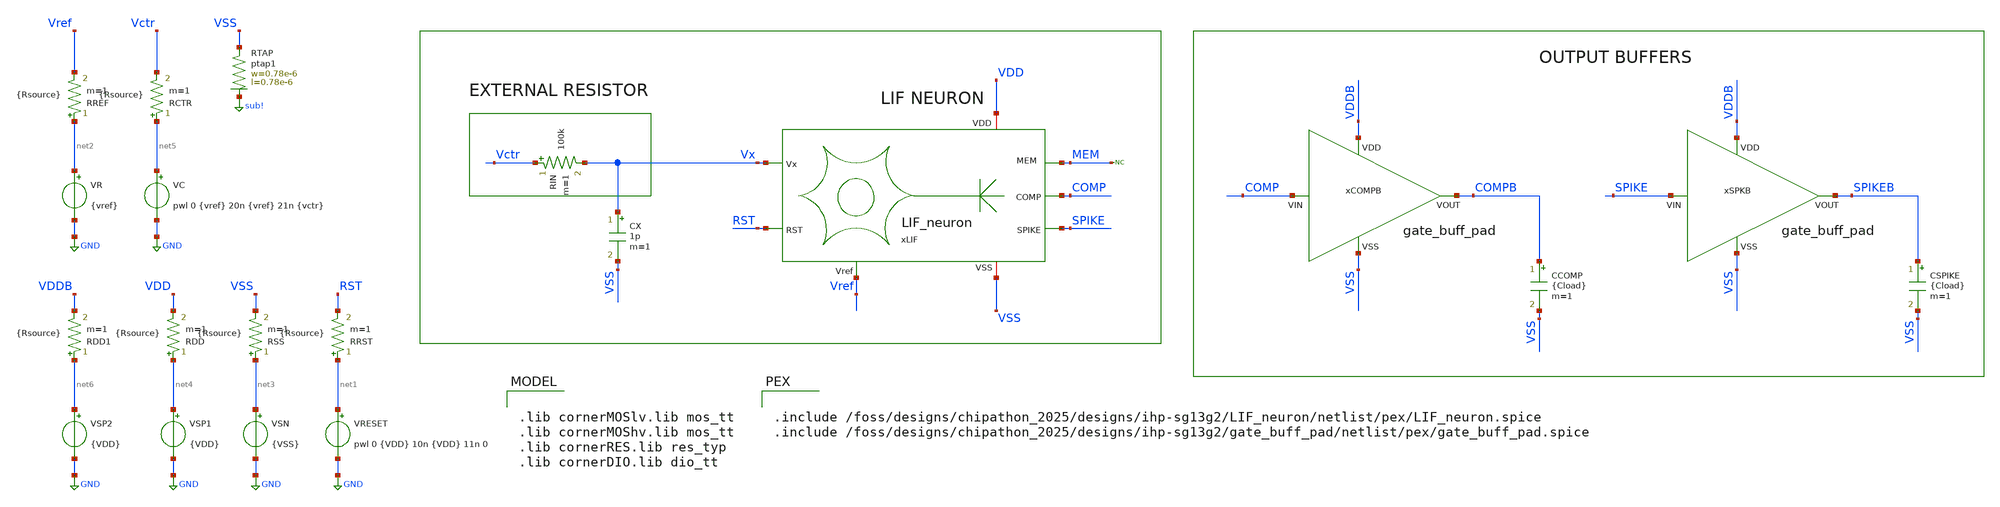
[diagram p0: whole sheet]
** sch_path: work/LIF_neuron/xschem/LIF_Neuron_tb_current.sch
**.subckt LIF_Neuron_tb_current
VRESET net1 GND pwl 0 {VDD} 10n {VDD} 11n 0
VSN net3 GND {VSS}
VR net2 GND {vref}
VC net5 GND pwl 0 {vref} 20n {vref} 21n {vctr}
xLIF VDD Vx MEM RST SPIKE VSS Vref COMP LIF_neuron
RDD net4 VDD {Rsource} m=1
RSS net3 VSS {Rsource} m=1
RRST net1 RST {Rsource} m=1
RREF net2 Vref {Rsource} m=1
RCTR net5 Vctr {Rsource} m=1
CSPIKE SPIKEB VSS {Cload} m=1
RIN Vctr Vx 100k m=1
VSP1 net4 GND {VDD}
* noconn MEM
XRTAP VSS sub! ptap1 R=262.8 w=0.78e-6 l=0.78e-6
xSPKB VDDB SPIKE SPIKEB VSS gate_buff_pad
xCOMPB VDDB COMP COMPB VSS gate_buff_pad
RDD1 net6 VDDB {Rsource} m=1
VSP2 net6 GND {VDD}
CX Vx VSS 1p m=1
CCOMP COMPB VSS {Cload} m=1
**** begin user architecture code



.temp 27
.param VDD = 0.6
.param VSS = 0
.param vctr = 0
.param vref = 0.6
.param Cload = 20p
.param Rsource = 1

.param sw_stat_global = 0
.param sw_stat_mismatch = 0

*.save @v.xLIF.VINT[i]
*.save @v.xLIF.VCOMP[i]
*.save @v.xLIF.VSPIKE[i]

.save all

.control

* >> Variables <<
let Vhigh = 0.5
let Vmid = Vhigh * 0.5
let tstop = 0.1u
let tstep = tstop/10k

* Run transient analysis
tran $&tstep $&tstop uic

* Average current
let IDD = -1*i(VSP1)
let IBUF = -1*i(VSP2)*0.5

meas tran I_avg AVG IDD from=11n to=tstop
let P_avg = abs(I_avg*Vhigh)
meas tran I_buf AVG IBUF from=11n to=tstop
let P_buf = abs(I_buf*Vhigh)

meas TRAN T_spk TRIG v(SPIKE) VAL=Vmid rise=2 TARG v(SPIKE) VAL=Vmid rise=3
let F_spk = 1 / T_spk
let E_spk = P_avg/F_spk

*Print Neuron results
print F_spk I_avg P_avg E_spk

*Internal currents
*let i_VINT = @v.xLIF.VINT[i]
*let i_VCOMP = @v.xLIF.VCOMP[i]
*let i_VSPIKE = @v.xLIF.VSPIKE[i]

*meas tran i_VINT AVG i_VINT from=11n to=tstop
*meas tran i_VCOMP AVG i_VCOMP from=11n to=tstop
*meas tran i_VSPIKE AVG i_VSPIKE from=11n to=tstop
*print i_VINT i_VCOMP i_VSPIKE

* Plots
plot v(Vctr) v(Vref) v(RST)
plot v(MEM) v(Vx) v(vctr)
plot v(COMP) v(SPIKE)
plot v(COMPB) v(SPIKEB)

.endc



.lib cornerMOSlv.lib mos_tt
.lib cornerMOShv.lib mos_tt
.lib cornerRES.lib res_typ
.lib cornerDIO.lib dio_tt


.include /foss/designs/chipathon_2025/designs/ihp-sg13g2/LIF_neuron/netlist/pex/LIF_neuron.spice
.include /foss/designs/chipathon_2025/designs/ihp-sg13g2/gate_buff_pad/netlist/pex/gate_buff_pad.spice

**** end user architecture code
**.ends
.GLOBAL GND
.GLOBAL sub!
.end
